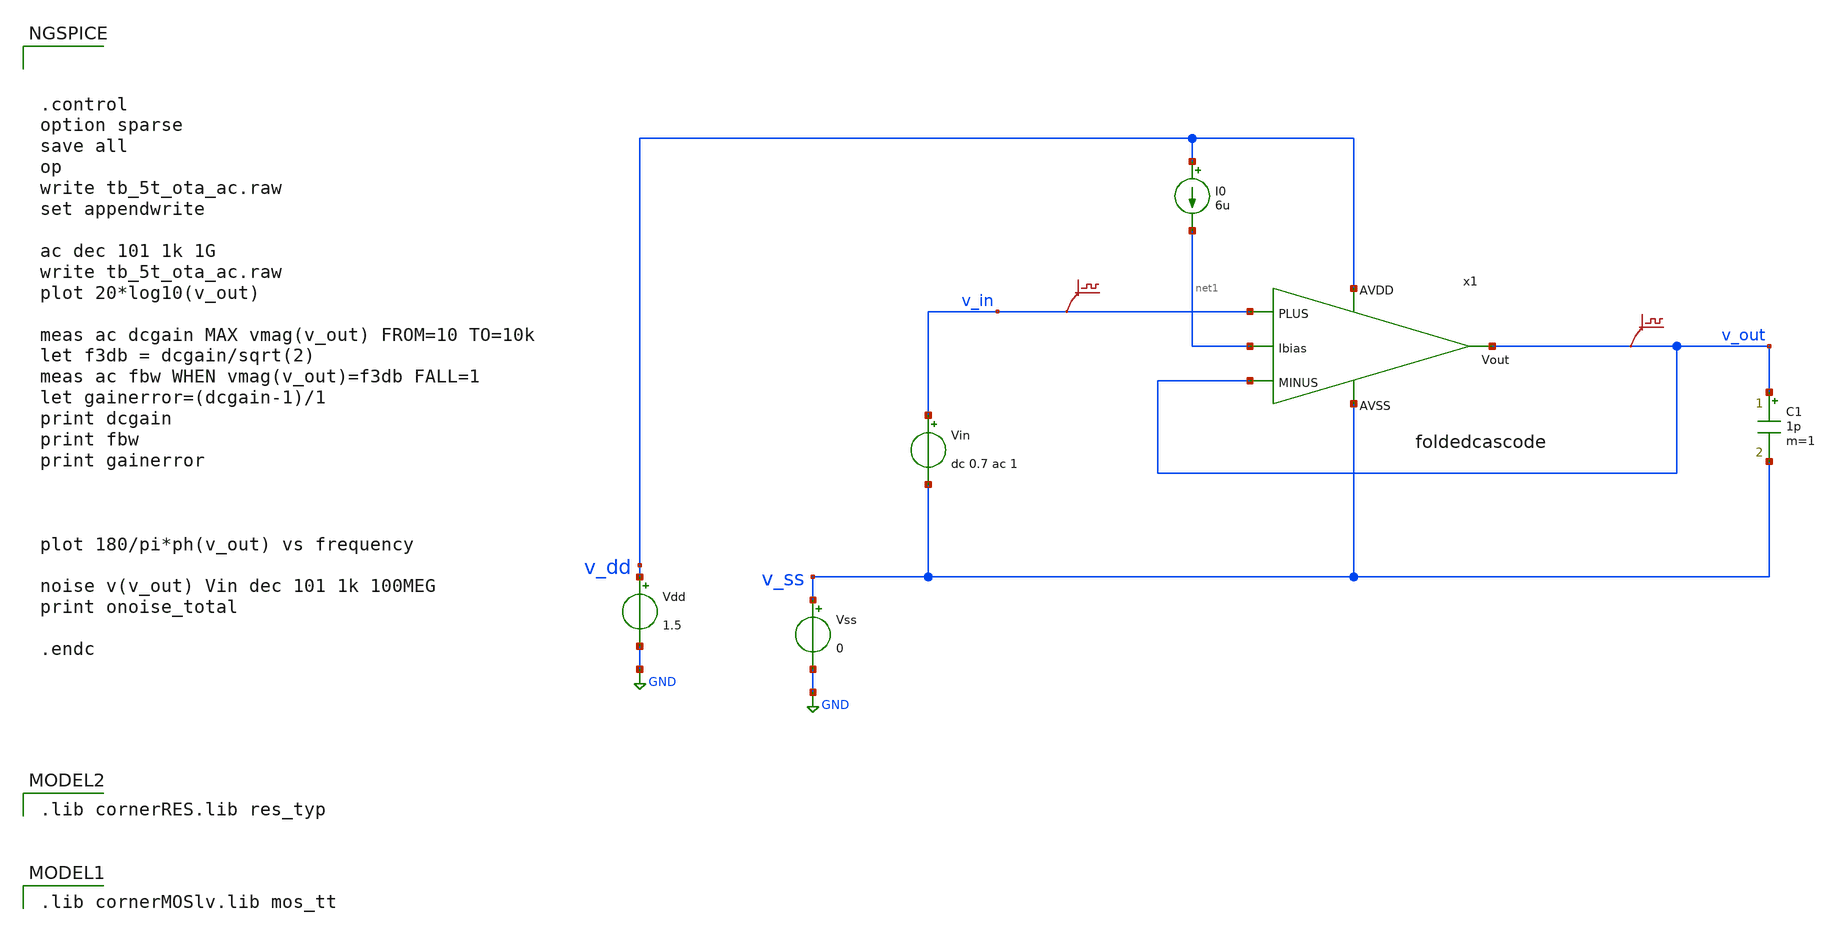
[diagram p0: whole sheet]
** sch_path: Designs/otas/tb_foldedcascode_ac.sch
* (c) 2025 Thesis_HP, Apache-2.0 license
**.subckt tb_foldedcascode_ac
Vss v_ss GND 0
Vdd v_dd GND 1.5
Vin v_in v_ss dc 0.7 ac 1
.save v(v_in)
I0 v_dd net1 6u
C1 v_out v_ss 1p m=1
.save v(v_out)
x1 v_dd net1 v_in v_out v_out v_ss foldedcascode
**** begin user architecture code
 .lib cornerMOSlv.lib mos_tt

 .lib cornerRES.lib res_typ




.control
option sparse
save all
op
write tb_5t_ota_ac.raw
set appendwrite

ac dec 101 1k 1G
write tb_5t_ota_ac.raw
plot 20*log10(v_out)

meas ac dcgain MAX vmag(v_out) FROM=10 TO=10k
let f3db = dcgain/sqrt(2)
meas ac fbw WHEN vmag(v_out)=f3db FALL=1
let gainerror=(dcgain-1)/1
print dcgain
print fbw
print gainerror



plot 180/pi*ph(v_out) vs frequency

noise v(v_out) Vin dec 101 1k 100MEG
print onoise_total

.endc


**** end user architecture code
**.ends

* expanding   symbol:  /foss/designs/thesis/workspace/thesis_hp/designs/5t_ota/foldedcascode.sym #
*+ of pins=6
** sym_path: Designs/otas/foldedcascode.sym
** sch_path: Designs/otas/foldedcascode.sch
.subckt foldedcascode AVDD Ibias PLUS MINUS Vout AVSS
*.ipin PLUS
*.ipin MINUS
*.opin Vout
*.ipin AVDD
*.ipin AVSS
*.ipin Ibias
XM1 net3 net10 AVDD AVDD sg13_lv_pmos w=0.56u l=0.5u ng=1 m=1 mm_ok=1
XM2 net2 PLUS net3 AVDD sg13_lv_pmos w=0.28u l=0.5u ng=1 m=1 mm_ok=1
XM3 net5 MINUS net3 AVDD sg13_lv_pmos w=0.28u l=0.5u ng=1 m=1 mm_ok=1
XM4 net4 net10 AVDD AVDD sg13_lv_pmos w=0.28u l=0.5u ng=1 m=1 mm_ok=1
XM5 Vout net1 net4 AVDD sg13_lv_pmos w=0.28u l=0.5u ng=1 m=1 mm_ok=1
XM14 net5 net8 AVSS AVSS sg13_lv_nmos w=0.54u l=0.5u ng=1 m=1 mm_ok=1
XM13 Vout net1 net5 AVSS sg13_lv_nmos w=0.27u l=0.5u ng=1 m=1 mm_ok=1
XM11 net6 net1 net2 AVSS sg13_lv_nmos w=0.27u l=0.5u ng=1 m=1 mm_ok=1
XM12 net2 net8 AVSS AVSS sg13_lv_nmos w=0.54u l=0.5u ng=1 m=1 mm_ok=1
XM17 net9 net8 AVSS AVSS sg13_lv_nmos w=0.27u l=0.5u ng=1 m=1 mm_ok=1
XM18 net1 net1 net9 AVSS sg13_lv_nmos w=0.27u l=0.5u ng=1 m=1 mm_ok=1
XM16 Ibias net1 net8 AVSS sg13_lv_nmos w=0.27u l=0.5u ng=1 m=1 mm_ok=1
XM15 net8 net8 AVSS AVSS sg13_lv_nmos w=0.27u l=0.5u ng=1 m=1 mm_ok=1
XM10 net6 net1 net7 AVDD sg13_lv_pmos w=0.28u l=0.5u ng=1 m=1 mm_ok=1
XM9 net7 net10 AVDD AVDD sg13_lv_pmos w=0.28u l=0.5u ng=1 m=1 mm_ok=1
XM19 net1 net1 net10 AVDD sg13_lv_pmos w=0.28u l=0.5u ng=1 m=1 mm_ok=1
XM20 net10 net10 AVDD AVDD sg13_lv_pmos w=0.28u l=0.5u ng=1 m=1 mm_ok=1
.ends

.GLOBAL GND
.end
